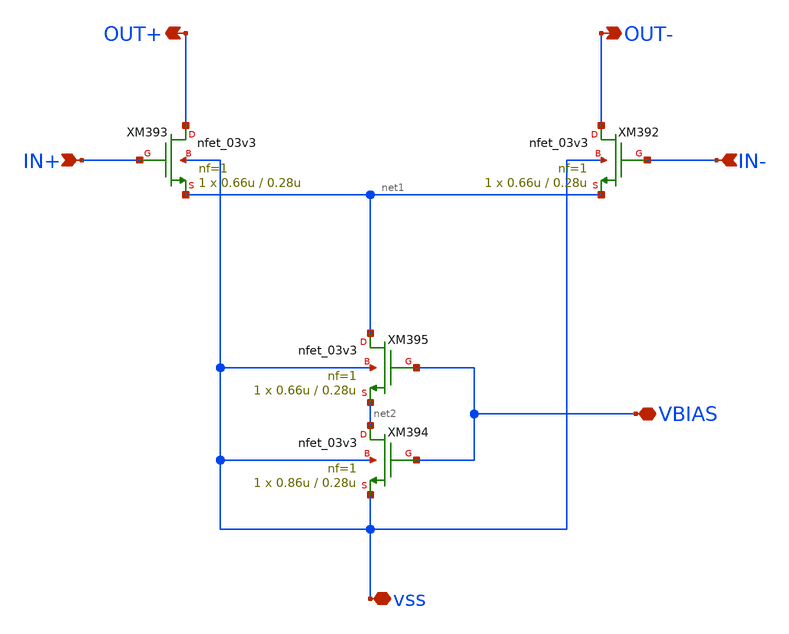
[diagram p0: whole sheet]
** sch_path: xschem/CS_Switch_8x.sch
**.subckt CS_Switch_8x OUT+ OUT- IN+ IN- VBIAS vss
*.opin OUT+
*.opin OUT-
*.ipin IN+
*.ipin IN-
*.iopin VBIAS
*.iopin vss
XM392 OUT- IN- net1 vss nfet_03v3 L=0.28u W=0.66u nf=1 ad='int((nf+1)/2) * W/nf * 0.18u' as='int((nf+2)/2) * W/nf * 0.18u'
+ pd='2*int((nf+1)/2) * (W/nf + 0.18u)' ps='2*int((nf+2)/2) * (W/nf + 0.18u)' nrd='0.18u / W' nrs='0.18u / W'
+ sa=0 sb=0 sd=0 m=1
XM393 OUT+ IN+ net1 vss nfet_03v3 L=0.28u W=0.66u nf=1 ad='int((nf+1)/2) * W/nf * 0.18u' as='int((nf+2)/2) * W/nf * 0.18u'
+ pd='2*int((nf+1)/2) * (W/nf + 0.18u)' ps='2*int((nf+2)/2) * (W/nf + 0.18u)' nrd='0.18u / W' nrs='0.18u / W'
+ sa=0 sb=0 sd=0 m=1
XM394 net2 VBIAS vss vss nfet_03v3 L=0.28u W=0.86u nf=1 ad='int((nf+1)/2) * W/nf * 0.18u' as='int((nf+2)/2) * W/nf * 0.18u'
+ pd='2*int((nf+1)/2) * (W/nf + 0.18u)' ps='2*int((nf+2)/2) * (W/nf + 0.18u)' nrd='0.18u / W' nrs='0.18u / W'
+ sa=0 sb=0 sd=0 m=1
XM395 net1 VBIAS net2 vss nfet_03v3 L=0.28u W=0.66u nf=1 ad='int((nf+1)/2) * W/nf * 0.18u' as='int((nf+2)/2) * W/nf * 0.18u'
+ pd='2*int((nf+1)/2) * (W/nf + 0.18u)' ps='2*int((nf+2)/2) * (W/nf + 0.18u)' nrd='0.18u / W' nrs='0.18u / W'
+ sa=0 sb=0 sd=0 m=1
**.ends
.end
